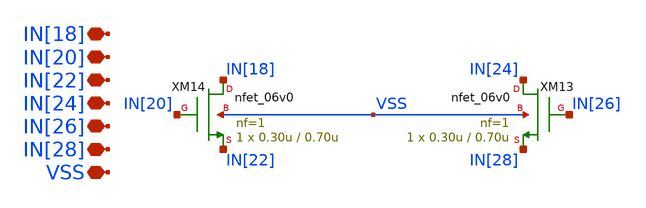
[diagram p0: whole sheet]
** sch_path: designs/libs/core_single-fet/nfet-vss/nfet-vss.sch
**.subckt nfet-vss VSS IN[28] IN[26] IN[24] IN[22] IN[20] IN[18]
*.iopin VSS
*.iopin IN[28]
*.iopin IN[26]
*.iopin IN[24]
*.iopin IN[22]
*.iopin IN[20]
*.iopin IN[18]
XM13 IN[24] IN[26] IN[28] VSS nfet_06v0 L=0.70u W=0.30u nf=1 ad='int((nf+1)/2) * W/nf * 0.18u' as='int((nf+2)/2) * W/nf * 0.18u'
+ pd='2*int((nf+1)/2) * (W/nf + 0.18u)' ps='2*int((nf+2)/2) * (W/nf + 0.18u)' nrd='0.18u / W' nrs='0.18u / W'
+ sa=0 sb=0 sd=0 m=1
XM14 IN[18] IN[20] IN[22] VSS nfet_06v0 L=0.70u W=0.30u nf=1 ad='int((nf+1)/2) * W/nf * 0.18u' as='int((nf+2)/2) * W/nf * 0.18u'
+ pd='2*int((nf+1)/2) * (W/nf + 0.18u)' ps='2*int((nf+2)/2) * (W/nf + 0.18u)' nrd='0.18u / W' nrs='0.18u / W'
+ sa=0 sb=0 sd=0 m=1
**.ends
.end
